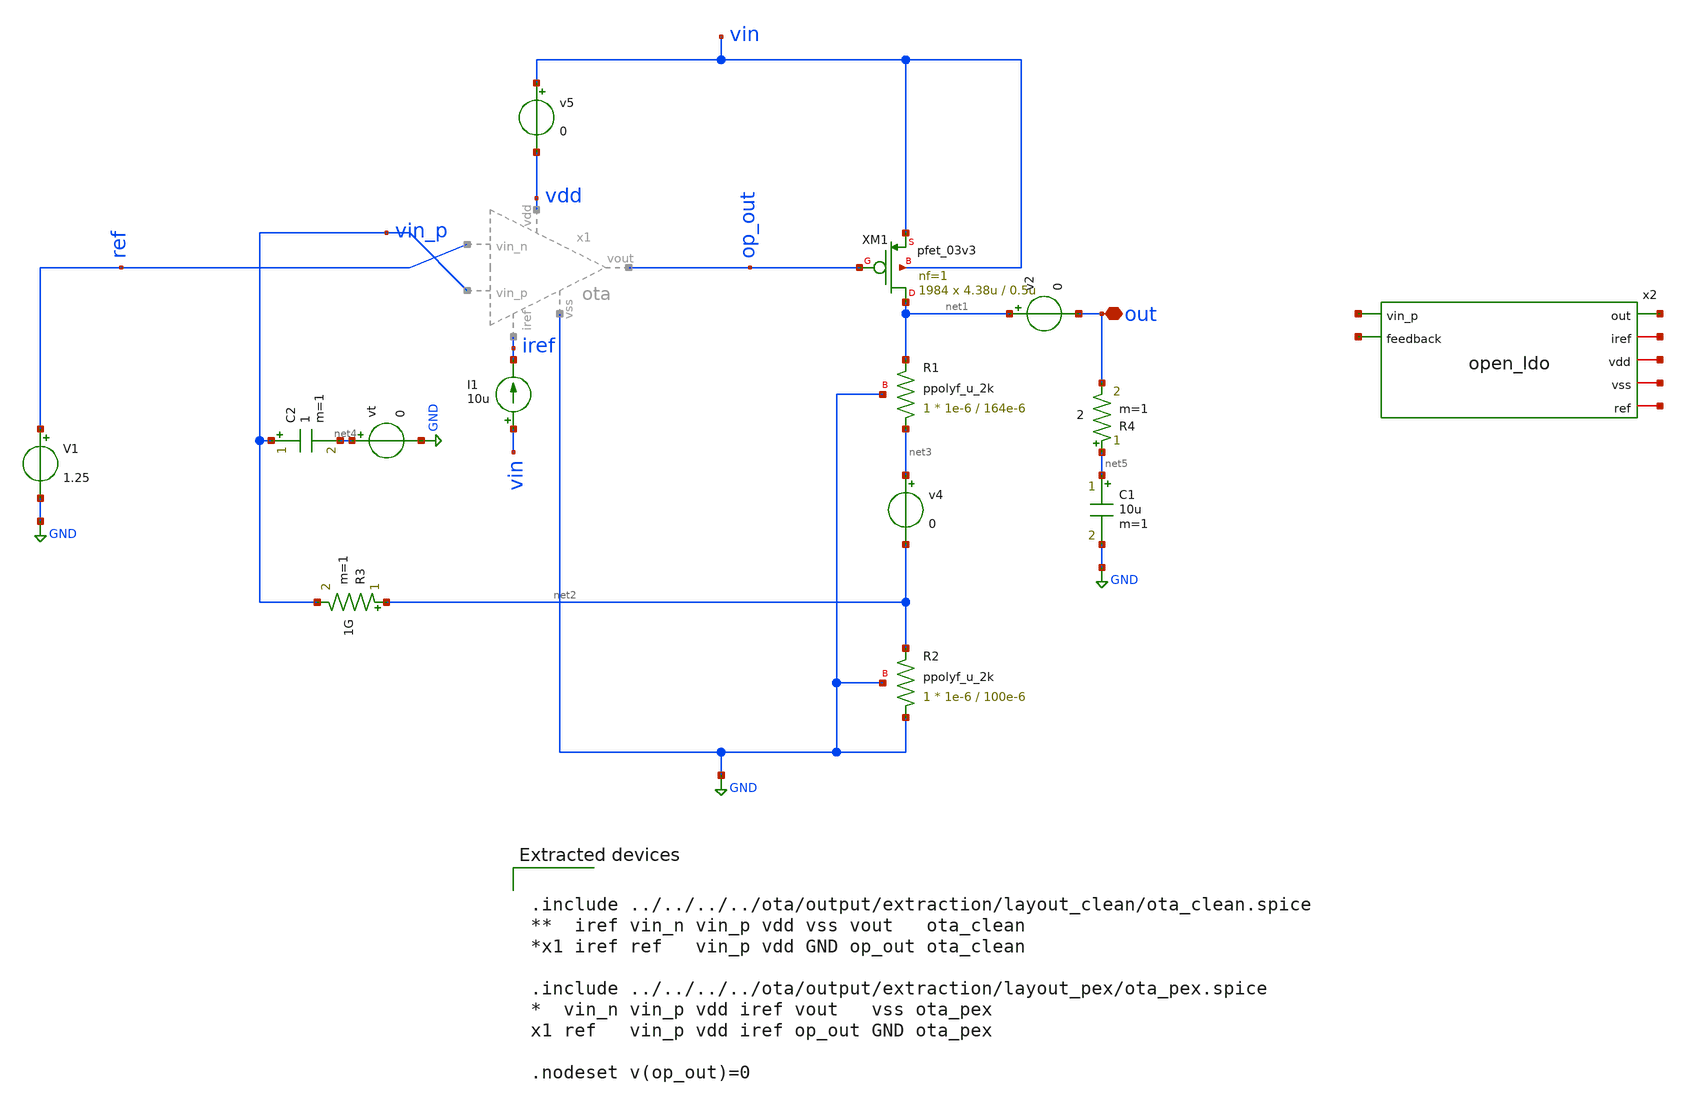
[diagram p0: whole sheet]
** sch_path: LDO/xschem/open_ldo/test/openloop.sch

.include $env(PDK_ROOT)/$env(PDK)/libs.tech/ngspice/design.ngspice
.lib $env(PDK_ROOT)/$env(PDK)/libs.tech/ngspice/sm141064.ngspice typical
.lib $env(PDK_ROOT)/$env(PDK)/libs.tech/ngspice/sm141064.ngspice res_typical

.lib $env(PDK_ROOT)/$env(PDK)/libs.tech/ngspice/sm141064.ngspice cap_mim
.lib $env(PDK_ROOT)/$env(PDK)/libs.tech/ngspice/sm141064.ngspice mimcap_typical

**.subckt openloop out
*.iopin out
I1 vin iref 10u
V1 ref GND 1.25
XM1 net1 op_out vin vin pfet_03v3 L=0.5u W=4.38u nf=1 ad='int((nf+1)/2) * W/nf * 0.18u' as='int((nf+2)/2) * W/nf * 0.18u'
+ pd='2*int((nf+1)/2) * (W/nf + 0.18u)' ps='2*int((nf+2)/2) * (W/nf + 0.18u)' nrd='0.18u / W' nrs='0.18u / W'
+ sa=0 sb=0 sd=0 m=1984
XR1 net3 net1 GND ppolyf_u_2k r_width=1e-6 r_length=164e-6 m=1
XR2 GND net2 GND ppolyf_u_2k r_width=1e-6 r_length=100e-6 m=1
v4 net3 net2 0
vt net4 GND 0
v2 net1 out 0
v5 vin vdd 0
R3 net2 vin_p 1G m=1
C2 vin_p net4 1 m=1
C1 net5 GND 10u m=1
R4 net5 out 2 m=1
x2 net6 net7 net8 net9 net10 net11 net12 open_ldo
**** begin user architecture code


.param R=66k
*.param R=33

Vs vin 0 5

.nodeset v(out)=0
.nodeset v(x1.pos)=0

*Stability_Analysis (openloop)
.control
reset
alter Vs AC=0
alter Vt AC =1
ac dec 100 1 1G
let phase_val = 180/PI*cph(out)
plot phase_val vdb(out)
meas ac pm FIND phase_val WHEN vdb(out)=0
meas ac cut_freq FIND frequency WHEN vdb(out)=0
*plot (180/pi)*vp(out)
*let gm0=@m.xm0.m0[gm]
*let Zout=(1.5)/(gm0*v(op_out))
*let Zout2=v(out)/gm0
*plot vdb(Zout2)
*wrdata /foss/designs/LDO_Design/data/data_PSRR.dat vdb(out)


op
print @m.x1.xm8.m0[vgs]-@m.x1.xm8.m0[vth]
print @m.x1.xm8.m0[vds]
print @m.x1.xm8.m0[id]
print **************
print @m.x1.xm7.m0[vgs]-@m.x1.xm7.m0[vth]
print @m.x1.xm7.m0[vds]
print @m.x1.xm7.m0[id]
print **************
print @m.x1.xm6.m0[vgs]-@m.x1.xm6.m0[vth]
print @m.x1.xm6.m0[vds]
print @m.x1.xm6.m0[gm]
print @m.x1.xm6.m0[gm]/@m.x1.xm6.m0[id]
print **************
print @m.x1.xm5.m0[vgs]-@m.x1.xm5.m0[vth]
print @m.x1.xm5.m0[vds]
print @m.x1.xm5.m0[id]
print **************
print @m.x1.xm1.m0[vgs]-@m.x1.xm1.m0[vth]
print @m.x1.xm1.m0[vds]
print @m.x1.xm1.m0[id]
print @m.x1.xm1.m0[gm]
print @m.x1.xm1.m0[gm]/@m.x1.xm1.m0[id]
print **************
print @m.x1.xm2.m0[vgs]-@m.x1.xm2.m0[vth]
print @m.x1.xm2.m0[vds]
print @m.x1.xm2.m0[id]
print @m.x1.xm2.m0[gm]
print @m.x1.xm2.m0[gm]/@m.x1.xm2.m0[id]
print **************
print @m.x1.xm3.m0[vgs]-@m.x1.xm3.m0[vth]
print @m.x1.xm3.m0[vds]
print @m.x1.xm3.m0[id]
print **************
print @m.x1.xm4.m0[vgs]-@m.x1.xm4.m0[vth]
print @m.x1.xm4.m0[vds]
print @m.x1.xm4.m0[id]

print v(op_out)
print v(out)

.endc




.include ../../../../ota/output/extraction/layout_clean/ota_clean.spice
**  iref vin_n vin_p vdd vss vout   ota_clean
*x1 iref ref   vin_p vdd GND op_out ota_clean

.include ../../../../ota/output/extraction/layout_pex/ota_pex.spice
*  vin_n vin_p vdd iref vout   vss ota_pex
x1 ref   vin_p vdd iref op_out GND ota_pex

.nodeset v(op_out)=0


**** end user architecture code
**.ends
.GLOBAL GND
.end
